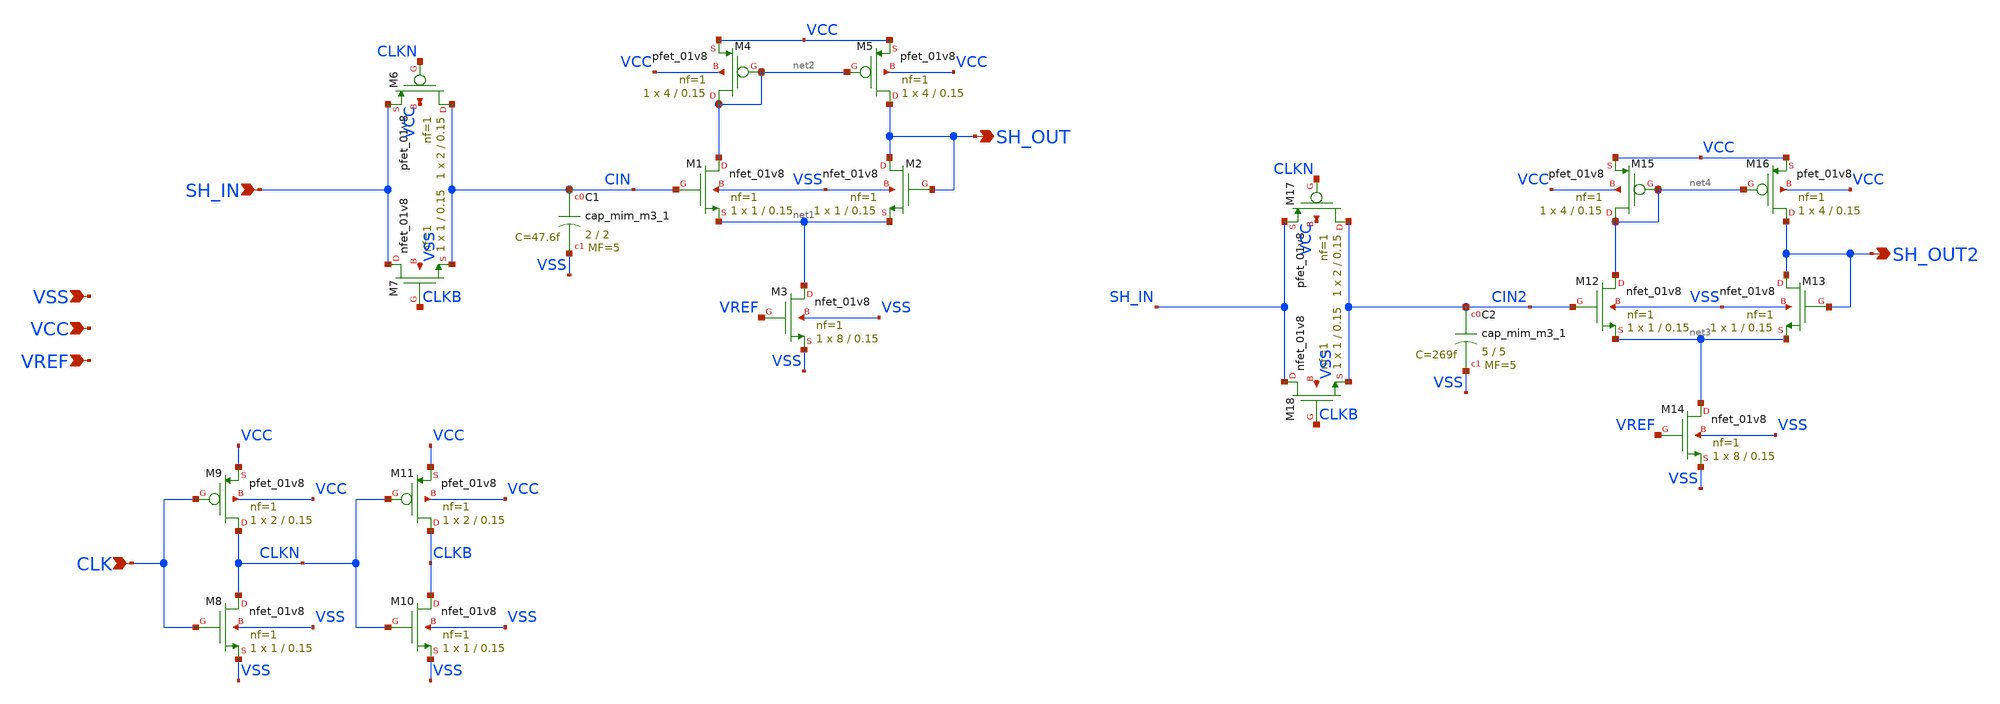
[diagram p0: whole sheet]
** sch_path: xschem/Sample_and_Hold.sch
**.subckt Sample_and_Hold SH_IN CLK SH_OUT VSS VCC SH_OUT2 VREF
*.ipin SH_IN
*.ipin CLK
*.opin SH_OUT
*.ipin VSS
*.ipin VCC
*.opin SH_OUT2
*.ipin VREF
XM1 net2 CIN net1 VSS sky130_fd_pr__nfet_01v8 L=0.15 W=1 nf=1 ad='int((nf+1)/2) * W/nf * 0.29' as='int((nf+2)/2) * W/nf * 0.29'
+ pd='2*int((nf+1)/2) * (W/nf + 0.29)' ps='2*int((nf+2)/2) * (W/nf + 0.29)' nrd='0.29 / W' nrs='0.29 / W'
+ sa=0 sb=0 sd=0 mult=1 m=1
XM2 SH_OUT SH_OUT net1 VSS sky130_fd_pr__nfet_01v8 L=0.15 W=1 nf=1 ad='int((nf+1)/2) * W/nf * 0.29' as='int((nf+2)/2) * W/nf * 0.29'
+ pd='2*int((nf+1)/2) * (W/nf + 0.29)' ps='2*int((nf+2)/2) * (W/nf + 0.29)' nrd='0.29 / W' nrs='0.29 / W'
+ sa=0 sb=0 sd=0 mult=1 m=1
XM3 net1 VREF VSS VSS sky130_fd_pr__nfet_01v8 L=0.15 W=8 nf=1 ad='int((nf+1)/2) * W/nf * 0.29' as='int((nf+2)/2) * W/nf * 0.29'
+ pd='2*int((nf+1)/2) * (W/nf + 0.29)' ps='2*int((nf+2)/2) * (W/nf + 0.29)' nrd='0.29 / W' nrs='0.29 / W'
+ sa=0 sb=0 sd=0 mult=1 m=1
XM4 net2 net2 VCC VCC sky130_fd_pr__pfet_01v8 L=0.15 W=4 nf=1 ad='int((nf+1)/2) * W/nf * 0.29' as='int((nf+2)/2) * W/nf * 0.29'
+ pd='2*int((nf+1)/2) * (W/nf + 0.29)' ps='2*int((nf+2)/2) * (W/nf + 0.29)' nrd='0.29 / W' nrs='0.29 / W'
+ sa=0 sb=0 sd=0 mult=1 m=1
XM5 SH_OUT net2 VCC VCC sky130_fd_pr__pfet_01v8 L=0.15 W=4 nf=1 ad='int((nf+1)/2) * W/nf * 0.29' as='int((nf+2)/2) * W/nf * 0.29'
+ pd='2*int((nf+1)/2) * (W/nf + 0.29)' ps='2*int((nf+2)/2) * (W/nf + 0.29)' nrd='0.29 / W' nrs='0.29 / W'
+ sa=0 sb=0 sd=0 mult=1 m=1
XC1 CIN VSS sky130_fd_pr__cap_mim_m3_1 W=2 L=2 MF=5 m=5
XM6 CIN CLKN SH_IN VCC sky130_fd_pr__pfet_01v8 L=0.15 W=2 nf=1 ad='int((nf+1)/2) * W/nf * 0.29' as='int((nf+2)/2) * W/nf * 0.29'
+ pd='2*int((nf+1)/2) * (W/nf + 0.29)' ps='2*int((nf+2)/2) * (W/nf + 0.29)' nrd='0.29 / W' nrs='0.29 / W'
+ sa=0 sb=0 sd=0 mult=1 m=1
XM7 SH_IN CLKB CIN VSS sky130_fd_pr__nfet_01v8 L=0.15 W=1 nf=1 ad='int((nf+1)/2) * W/nf * 0.29' as='int((nf+2)/2) * W/nf * 0.29'
+ pd='2*int((nf+1)/2) * (W/nf + 0.29)' ps='2*int((nf+2)/2) * (W/nf + 0.29)' nrd='0.29 / W' nrs='0.29 / W'
+ sa=0 sb=0 sd=0 mult=1 m=1
XM8 CLKN CLK VSS VSS sky130_fd_pr__nfet_01v8 L=0.15 W=1 nf=1 ad='int((nf+1)/2) * W/nf * 0.29' as='int((nf+2)/2) * W/nf * 0.29'
+ pd='2*int((nf+1)/2) * (W/nf + 0.29)' ps='2*int((nf+2)/2) * (W/nf + 0.29)' nrd='0.29 / W' nrs='0.29 / W'
+ sa=0 sb=0 sd=0 mult=1 m=1
XM9 CLKN CLK VCC VCC sky130_fd_pr__pfet_01v8 L=0.15 W=2 nf=1 ad='int((nf+1)/2) * W/nf * 0.29' as='int((nf+2)/2) * W/nf * 0.29'
+ pd='2*int((nf+1)/2) * (W/nf + 0.29)' ps='2*int((nf+2)/2) * (W/nf + 0.29)' nrd='0.29 / W' nrs='0.29 / W'
+ sa=0 sb=0 sd=0 mult=1 m=1
XM10 CLKB CLKN VSS VSS sky130_fd_pr__nfet_01v8 L=0.15 W=1 nf=1 ad='int((nf+1)/2) * W/nf * 0.29' as='int((nf+2)/2) * W/nf * 0.29'
+ pd='2*int((nf+1)/2) * (W/nf + 0.29)' ps='2*int((nf+2)/2) * (W/nf + 0.29)' nrd='0.29 / W' nrs='0.29 / W'
+ sa=0 sb=0 sd=0 mult=1 m=1
XM11 CLKB CLKN VCC VCC sky130_fd_pr__pfet_01v8 L=0.15 W=2 nf=1 ad='int((nf+1)/2) * W/nf * 0.29' as='int((nf+2)/2) * W/nf * 0.29'
+ pd='2*int((nf+1)/2) * (W/nf + 0.29)' ps='2*int((nf+2)/2) * (W/nf + 0.29)' nrd='0.29 / W' nrs='0.29 / W'
+ sa=0 sb=0 sd=0 mult=1 m=1
XC2 CIN2 VSS sky130_fd_pr__cap_mim_m3_1 W=5 L=5 MF=5 m=5
XM17 CIN2 CLKN SH_IN VCC sky130_fd_pr__pfet_01v8 L=0.15 W=2 nf=1 ad='int((nf+1)/2) * W/nf * 0.29' as='int((nf+2)/2) * W/nf * 0.29'
+ pd='2*int((nf+1)/2) * (W/nf + 0.29)' ps='2*int((nf+2)/2) * (W/nf + 0.29)' nrd='0.29 / W' nrs='0.29 / W'
+ sa=0 sb=0 sd=0 mult=1 m=1
XM18 SH_IN CLKB CIN2 VSS sky130_fd_pr__nfet_01v8 L=0.15 W=1 nf=1 ad='int((nf+1)/2) * W/nf * 0.29' as='int((nf+2)/2) * W/nf * 0.29'
+ pd='2*int((nf+1)/2) * (W/nf + 0.29)' ps='2*int((nf+2)/2) * (W/nf + 0.29)' nrd='0.29 / W' nrs='0.29 / W'
+ sa=0 sb=0 sd=0 mult=1 m=1
XM12 net4 CIN2 net3 VSS sky130_fd_pr__nfet_01v8 L=0.15 W=1 nf=1 ad='int((nf+1)/2) * W/nf * 0.29' as='int((nf+2)/2) * W/nf * 0.29'
+ pd='2*int((nf+1)/2) * (W/nf + 0.29)' ps='2*int((nf+2)/2) * (W/nf + 0.29)' nrd='0.29 / W' nrs='0.29 / W'
+ sa=0 sb=0 sd=0 mult=1 m=1
XM13 SH_OUT2 SH_OUT2 net3 VSS sky130_fd_pr__nfet_01v8 L=0.15 W=1 nf=1 ad='int((nf+1)/2) * W/nf * 0.29'
+ as='int((nf+2)/2) * W/nf * 0.29' pd='2*int((nf+1)/2) * (W/nf + 0.29)' ps='2*int((nf+2)/2) * (W/nf + 0.29)'
+ nrd='0.29 / W' nrs='0.29 / W' sa=0 sb=0 sd=0 mult=1 m=1
XM14 net3 VREF VSS VSS sky130_fd_pr__nfet_01v8 L=0.15 W=8 nf=1 ad='int((nf+1)/2) * W/nf * 0.29' as='int((nf+2)/2) * W/nf * 0.29'
+ pd='2*int((nf+1)/2) * (W/nf + 0.29)' ps='2*int((nf+2)/2) * (W/nf + 0.29)' nrd='0.29 / W' nrs='0.29 / W'
+ sa=0 sb=0 sd=0 mult=1 m=1
XM15 net4 net4 VCC VCC sky130_fd_pr__pfet_01v8 L=0.15 W=4 nf=1 ad='int((nf+1)/2) * W/nf * 0.29' as='int((nf+2)/2) * W/nf * 0.29'
+ pd='2*int((nf+1)/2) * (W/nf + 0.29)' ps='2*int((nf+2)/2) * (W/nf + 0.29)' nrd='0.29 / W' nrs='0.29 / W'
+ sa=0 sb=0 sd=0 mult=1 m=1
XM16 SH_OUT2 net4 VCC VCC sky130_fd_pr__pfet_01v8 L=0.15 W=4 nf=1 ad='int((nf+1)/2) * W/nf * 0.29' as='int((nf+2)/2) * W/nf * 0.29'
+ pd='2*int((nf+1)/2) * (W/nf + 0.29)' ps='2*int((nf+2)/2) * (W/nf + 0.29)' nrd='0.29 / W' nrs='0.29 / W'
+ sa=0 sb=0 sd=0 mult=1 m=1
**.ends
.end
